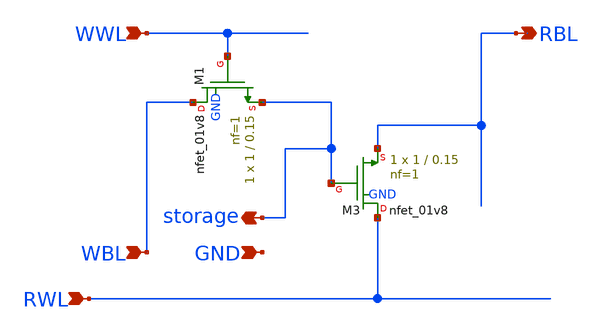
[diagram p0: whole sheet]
** sch_path: xschem/digital_prims/dram.sch
**.subckt dram RBL RWL WBL WWL storage GND
*.opin RBL
*.ipin RWL
*.ipin WBL
*.ipin WWL
*.opin storage
*.ipin GND
XM3 RWL storage RBL GND sky130_fd_pr__nfet_01v8 L=0.15 W=1 nf=1 ad='int((nf+1)/2) * W/nf * 0.29' as='int((nf+2)/2) * W/nf * 0.29'
+ pd='2*int((nf+1)/2) * (W/nf + 0.29)' ps='2*int((nf+2)/2) * (W/nf + 0.29)' nrd='0.29 / W' nrs='0.29 / W'
+ sa=0 sb=0 sd=0 mult=1 m=1
XM1 WBL WWL storage GND sky130_fd_pr__nfet_01v8 L=0.15 W=1 nf=1 ad='int((nf+1)/2) * W/nf * 0.29' as='int((nf+2)/2) * W/nf * 0.29'
+ pd='2*int((nf+1)/2) * (W/nf + 0.29)' ps='2*int((nf+2)/2) * (W/nf + 0.29)' nrd='0.29 / W' nrs='0.29 / W'
+ sa=0 sb=0 sd=0 mult=1 m=1
**.ends
.end
